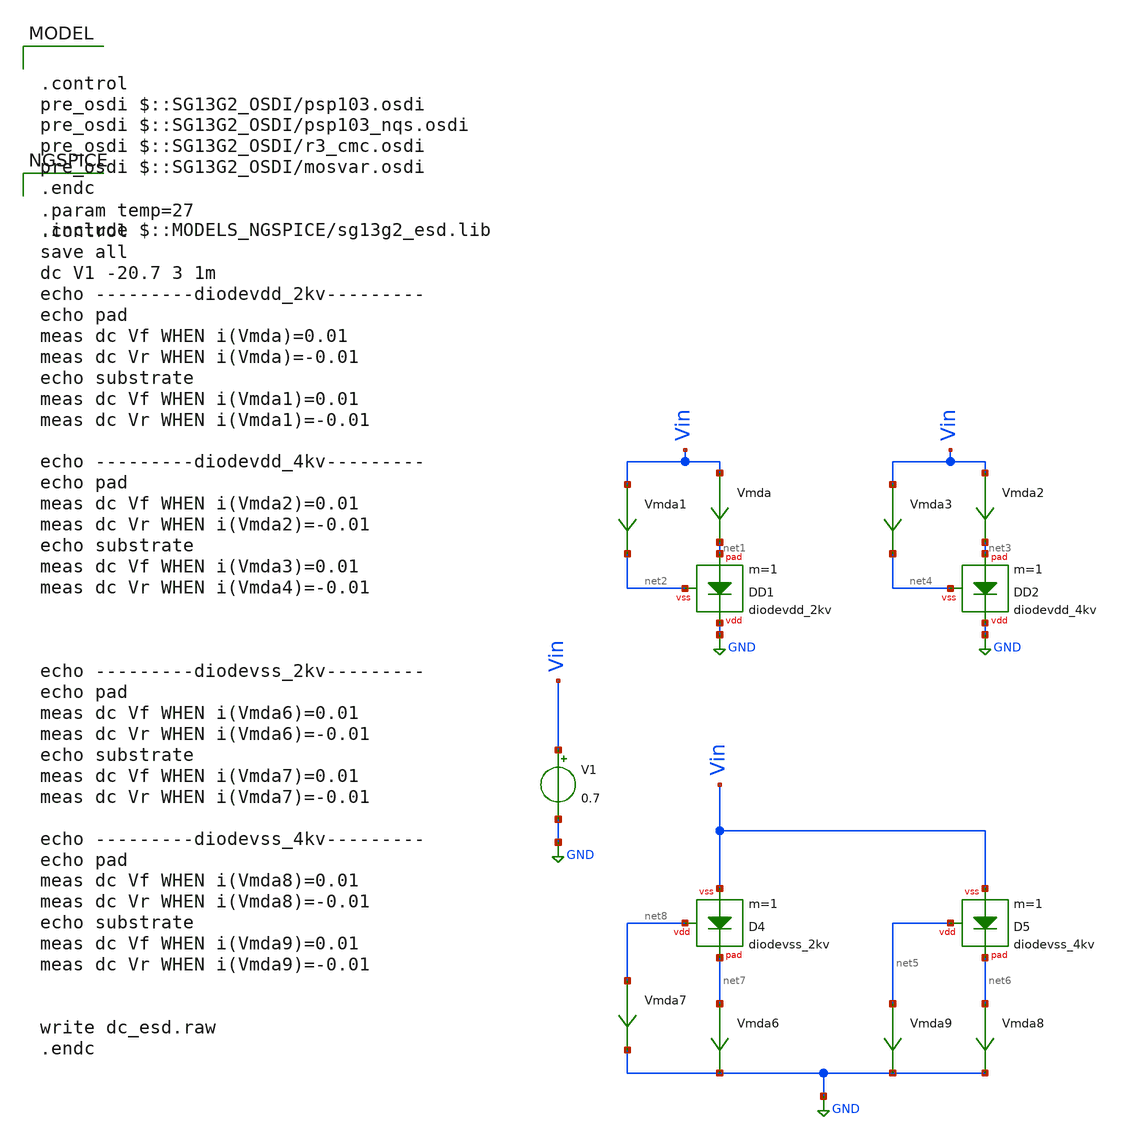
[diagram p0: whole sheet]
** sch_path: ihp-sg13g2/xschem_libs/sg13g2_tests/dc_esd_diodes/schematic/dc_esd_diodes.sch
**.subckt dc_esd_diodes
V1 Vin GND 0.7
Vmda Vin net1 0
.save i(vmda)
Vmda1 Vin net2 0
.save i(vmda1)
XD1 GND net1 net2 diodevdd_2kv m=1
Vmda2 Vin net3 0
.save i(vmda2)
Vmda3 Vin net4 0
.save i(vmda3)
XD2 GND net3 net4 diodevdd_4kv m=1
Vmda6 net7 GND 0
.save i(vmda6)
Vmda7 net8 GND 0
.save i(vmda7)
XD4 net8 net7 Vin diodevss_2kv m=1
Vmda8 net6 GND 0
.save i(vmda8)
Vmda9 net5 GND 0
.save i(vmda9)
XD5 net5 net6 Vin diodevss_4kv m=1
**** begin user architecture code

.control
pre_osdi $::SG13G2_OSDI/psp103.osdi
pre_osdi $::SG13G2_OSDI/psp103_nqs.osdi
pre_osdi $::SG13G2_OSDI/r3_cmc.osdi
pre_osdi $::SG13G2_OSDI/mosvar.osdi
.endc

.include $::MODELS_NGSPICE/sg13g2_esd.lib



.param temp=27
.control
save all
dc V1 -20.7 3 1m
echo ---------diodevdd_2kv---------
echo pad
meas dc Vf WHEN i(Vmda)=0.01
meas dc Vr WHEN i(Vmda)=-0.01
echo substrate
meas dc Vf WHEN i(Vmda1)=0.01
meas dc Vr WHEN i(Vmda1)=-0.01

echo ---------diodevdd_4kv---------
echo pad
meas dc Vf WHEN i(Vmda2)=0.01
meas dc Vr WHEN i(Vmda2)=-0.01
echo substrate
meas dc Vf WHEN i(Vmda3)=0.01
meas dc Vr WHEN i(Vmda4)=-0.01



echo ---------diodevss_2kv---------
echo pad
meas dc Vf WHEN i(Vmda6)=0.01
meas dc Vr WHEN i(Vmda6)=-0.01
echo substrate
meas dc Vf WHEN i(Vmda7)=0.01
meas dc Vr WHEN i(Vmda7)=-0.01

echo ---------diodevss_4kv---------
echo pad
meas dc Vf WHEN i(Vmda8)=0.01
meas dc Vr WHEN i(Vmda8)=-0.01
echo substrate
meas dc Vf WHEN i(Vmda9)=0.01
meas dc Vr WHEN i(Vmda9)=-0.01


write dc_esd.raw
.endc


**** end user architecture code
**.ends
.GLOBAL GND
.end
